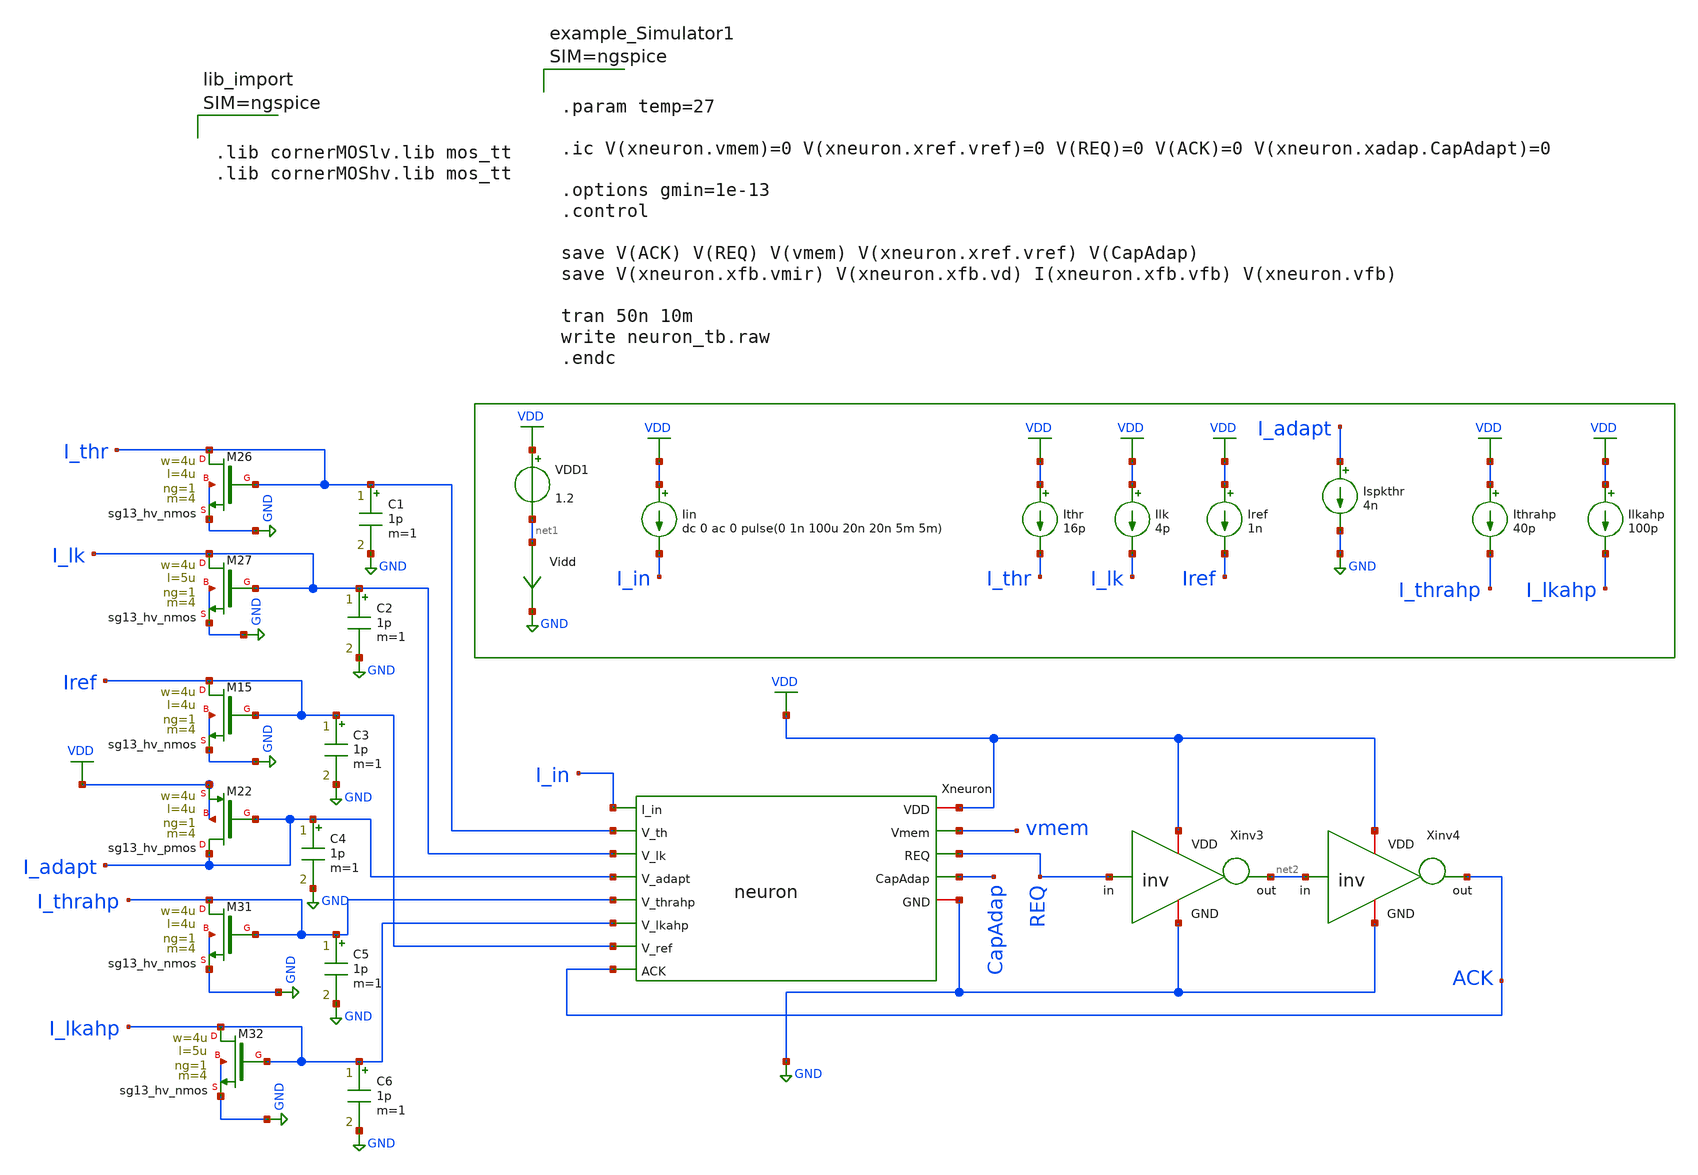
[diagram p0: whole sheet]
** sch_path: xschem/neuron_tb.sch
**.subckt neuron_tb
Xneuron VDD I_in I_thr I_lk vmem REQ I_adapt I_thrahp CapAdap ACK I_lkahp Iref GND neuron
Ithr VDD I_thr 16p
Ilk VDD I_lk 4p
Ispkthr I_adapt GND 4n
Iin VDD I_in dc 0 ac 0 pulse(0 1n 100u 20n 20n 5m 5m)
VDD1 VDD net1 1.2
Iref VDD Iref 1n
Vidd net1 GND 0
.save i(vidd)
Ilkahp VDD I_lkahp 100p
Ithrahp VDD I_thrahp 40p
XM26 I_thr I_thr GND GND sg13_hv_nmos w=4u l=4u ng=1 m=4 mm_ok=1
XM27 I_lk I_lk GND GND sg13_hv_nmos w=4u l=5u ng=1 m=4 mm_ok=1
XM15 Iref Iref GND GND sg13_hv_nmos w=4u l=4u ng=1 m=4 mm_ok=1
XM22 I_adapt I_adapt VDD VDD sg13_hv_pmos w=4u l=4u ng=1 m=4 mm_ok=1
XM31 I_thrahp I_thrahp GND GND sg13_hv_nmos w=4u l=4u ng=1 m=4 mm_ok=1
XM32 I_lkahp I_lkahp GND GND sg13_hv_nmos w=4u l=5u ng=1 m=4 mm_ok=1
Xinv3 VDD REQ net2 GND inv
Xinv4 VDD net2 ACK GND inv
C1 I_thr GND 1p m=1
C2 I_lk GND 1p m=1
C3 Iref GND 1p m=1
C4 I_adapt GND 1p m=1
C5 I_thrahp GND 1p m=1
C6 I_lkahp GND 1p m=1
**** begin user architecture code



.param temp=27

.ic V(xneuron.vmem)=0 V(xneuron.xref.vref)=0 V(REQ)=0 V(ACK)=0 V(xneuron.xadap.CapAdapt)=0

.options gmin=1e-13
.control

save V(ACK) V(REQ) V(vmem) V(xneuron.xref.vref) V(CapAdap)
save V(xneuron.xfb.vmir) V(xneuron.xfb.vd) I(xneuron.xfb.vfb) V(xneuron.vfb)

tran 50n 10m
write neuron_tb.raw
.endc







.lib cornerMOSlv.lib mos_tt
.lib cornerMOShv.lib mos_tt


**** end user architecture code
**.ends
.GLOBAL GND
.GLOBAL VDD
.end
